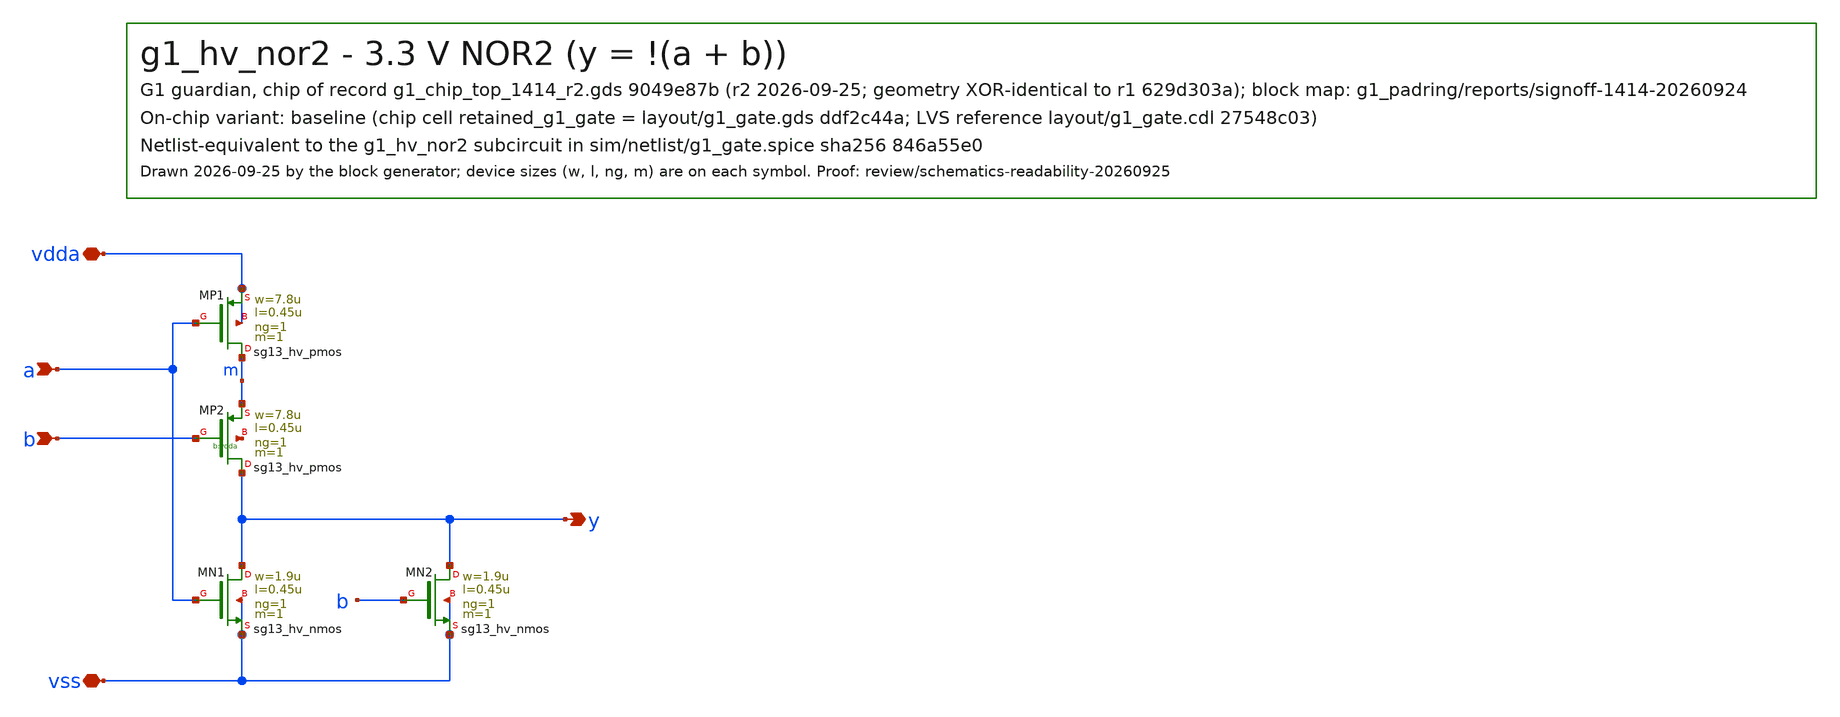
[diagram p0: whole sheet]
** sch_path: designs/g1-guardian/blocks/g1_gate/schematic/g1_hv_nor2.sch
**.subckt g1_hv_nor2 a b y vdda vss
*.ipin a
*.ipin b
*.opin y
*.iopin vdda
*.iopin vss
XMP1 m a vdda vdda sg13_hv_pmos w=7.8u l=0.45u ng=1 m=1 mm_ok=1
XMP2 y b m vdda sg13_hv_pmos w=7.8u l=0.45u ng=1 m=1 mm_ok=1
XMN1 y a vss vss sg13_hv_nmos w=1.9u l=0.45u ng=1 m=1 mm_ok=1
XMN2 y b vss vss sg13_hv_nmos w=1.9u l=0.45u ng=1 m=1 mm_ok=1
**.ends
.end
